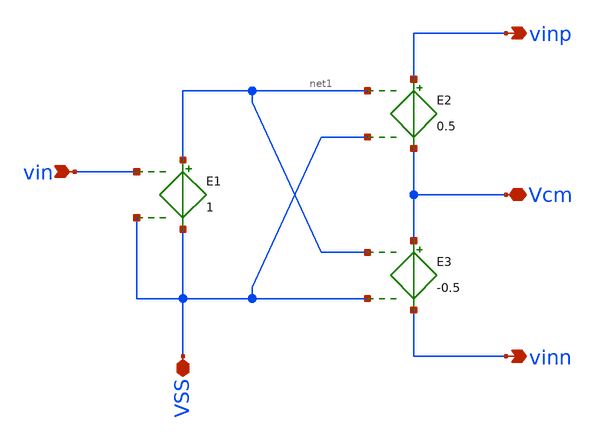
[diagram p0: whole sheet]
** sch_path: sky130/xschem/single2cm.sch
**.subckt single2cm vin vinn Vcm vinp VSS
*.ipin vin
*.opin vinn
*.iopin Vcm
*.opin vinp
*.iopin VSS
E3 Vcm vinn net1 VSS -0.5
E2 vinp Vcm net1 VSS 0.5
E1 net1 VSS vin VSS 1
**.ends
.end
